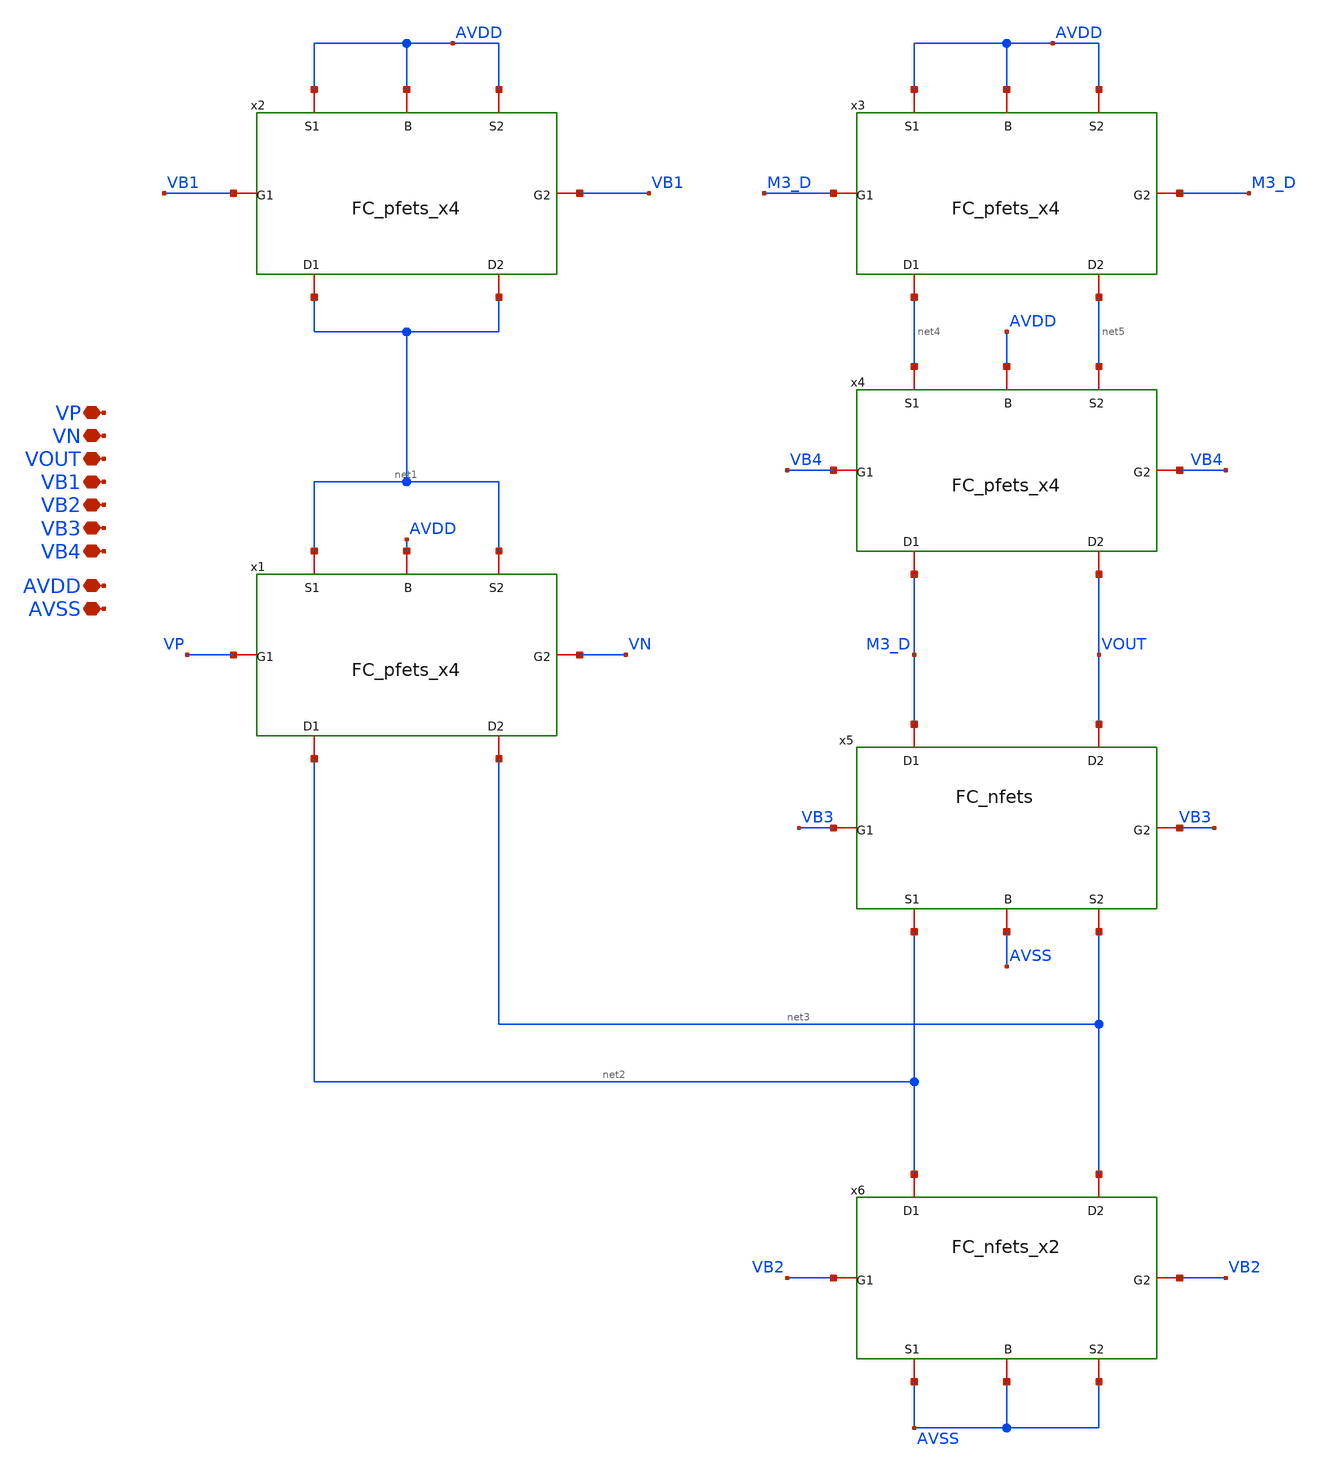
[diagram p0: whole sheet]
** sch_path: TIA_Filter/Folded/FC_net.sch
**.subckt FC_net AVDD AVSS VOUT VP VN VB1 VB2 VB3 VB4
*.iopin AVDD
*.iopin AVSS
*.iopin VOUT
*.iopin VP
*.iopin VN
*.iopin VB1
*.iopin VB2
*.iopin VB3
*.iopin VB4
x1 net1 net1 net2 net3 VP VN AVDD FC_pfets_x4
x2 AVDD AVDD net1 net1 VB1 VB1 AVDD FC_pfets_x4
x3 AVDD AVDD net4 net5 M3_D M3_D AVDD FC_pfets_x4
x4 net4 net5 M3_D VOUT VB4 VB4 AVDD FC_pfets_x4
x5 net2 net3 M3_D VOUT VB3 VB3 AVSS FC_nfets
x6 AVSS AVSS net2 net3 VB2 VB2 AVSS FC_nfets_x2
**.ends

* expanding   symbol:  /home/gmaranhao/Desktop/Bracolin/TIA_Filter/Folded/FC_pfets_x4.sym # of
*+ pins=7
** sym_path: TIA_Filter/Folded/FC_pfets_x4.sym
** sch_path: TIA_Filter/Folded/FC_pfets_x4.sch
.subckt FC_pfets_x4 S1 S2 D1 D2 G1 G2 B
*.iopin S1
*.iopin S2
*.iopin D1
*.iopin D2
*.iopin G1
*.iopin G2
*.iopin B
x1[1] S1 S2 D1 D2 G1 G2 B FC_pfets
x1[2] S1 S2 D1 D2 G1 G2 B FC_pfets
x1[3] S1 S2 D1 D2 G1 G2 B FC_pfets
x1[4] S1 S2 D1 D2 G1 G2 B FC_pfets
.ends


* expanding   symbol:  /home/gmaranhao/Desktop/Bracolin/TIA_Filter/Folded/FC_nfets.sym # of pins=7
** sym_path: TIA_Filter/Folded/FC_nfets.sym
** sch_path: TIA_Filter/Folded/FC_nfets.sch
.subckt FC_nfets S1 S2 D1 D2 G1 G2 B
*.iopin S1
*.iopin S2
*.iopin D1
*.iopin D2
*.iopin G1
*.iopin G2
*.iopin B
XM1[1] D1 G1 S1 B nfet_03v3 L=2u W=2u nf=1 ad='int((nf+1)/2) * W/nf * 0.18u' as='int((nf+2)/2) * W/nf * 0.18u'
+ pd='2*int((nf+1)/2) * (W/nf + 0.18u)' ps='2*int((nf+2)/2) * (W/nf + 0.18u)' nrd='0.18u / W' nrs='0.18u / W'
+ sa=0 sb=0 sd=0 m=1
XM1[2] D1 G1 S1 B nfet_03v3 L=2u W=2u nf=1 ad='int((nf+1)/2) * W/nf * 0.18u' as='int((nf+2)/2) * W/nf * 0.18u'
+ pd='2*int((nf+1)/2) * (W/nf + 0.18u)' ps='2*int((nf+2)/2) * (W/nf + 0.18u)' nrd='0.18u / W' nrs='0.18u / W'
+ sa=0 sb=0 sd=0 m=1
XM1[3] D1 G1 S1 B nfet_03v3 L=2u W=2u nf=1 ad='int((nf+1)/2) * W/nf * 0.18u' as='int((nf+2)/2) * W/nf * 0.18u'
+ pd='2*int((nf+1)/2) * (W/nf + 0.18u)' ps='2*int((nf+2)/2) * (W/nf + 0.18u)' nrd='0.18u / W' nrs='0.18u / W'
+ sa=0 sb=0 sd=0 m=1
XM1[4] D1 G1 S1 B nfet_03v3 L=2u W=2u nf=1 ad='int((nf+1)/2) * W/nf * 0.18u' as='int((nf+2)/2) * W/nf * 0.18u'
+ pd='2*int((nf+1)/2) * (W/nf + 0.18u)' ps='2*int((nf+2)/2) * (W/nf + 0.18u)' nrd='0.18u / W' nrs='0.18u / W'
+ sa=0 sb=0 sd=0 m=1
XM1[5] D1 G1 S1 B nfet_03v3 L=2u W=2u nf=1 ad='int((nf+1)/2) * W/nf * 0.18u' as='int((nf+2)/2) * W/nf * 0.18u'
+ pd='2*int((nf+1)/2) * (W/nf + 0.18u)' ps='2*int((nf+2)/2) * (W/nf + 0.18u)' nrd='0.18u / W' nrs='0.18u / W'
+ sa=0 sb=0 sd=0 m=1
XM1[6] D1 G1 S1 B nfet_03v3 L=2u W=2u nf=1 ad='int((nf+1)/2) * W/nf * 0.18u' as='int((nf+2)/2) * W/nf * 0.18u'
+ pd='2*int((nf+1)/2) * (W/nf + 0.18u)' ps='2*int((nf+2)/2) * (W/nf + 0.18u)' nrd='0.18u / W' nrs='0.18u / W'
+ sa=0 sb=0 sd=0 m=1
XM1[7] D1 G1 S1 B nfet_03v3 L=2u W=2u nf=1 ad='int((nf+1)/2) * W/nf * 0.18u' as='int((nf+2)/2) * W/nf * 0.18u'
+ pd='2*int((nf+1)/2) * (W/nf + 0.18u)' ps='2*int((nf+2)/2) * (W/nf + 0.18u)' nrd='0.18u / W' nrs='0.18u / W'
+ sa=0 sb=0 sd=0 m=1
XM1[8] D1 G1 S1 B nfet_03v3 L=2u W=2u nf=1 ad='int((nf+1)/2) * W/nf * 0.18u' as='int((nf+2)/2) * W/nf * 0.18u'
+ pd='2*int((nf+1)/2) * (W/nf + 0.18u)' ps='2*int((nf+2)/2) * (W/nf + 0.18u)' nrd='0.18u / W' nrs='0.18u / W'
+ sa=0 sb=0 sd=0 m=1
XM1[9] D1 G1 S1 B nfet_03v3 L=2u W=2u nf=1 ad='int((nf+1)/2) * W/nf * 0.18u' as='int((nf+2)/2) * W/nf * 0.18u'
+ pd='2*int((nf+1)/2) * (W/nf + 0.18u)' ps='2*int((nf+2)/2) * (W/nf + 0.18u)' nrd='0.18u / W' nrs='0.18u / W'
+ sa=0 sb=0 sd=0 m=1
XM1[10] D1 G1 S1 B nfet_03v3 L=2u W=2u nf=1 ad='int((nf+1)/2) * W/nf * 0.18u' as='int((nf+2)/2) * W/nf * 0.18u'
+ pd='2*int((nf+1)/2) * (W/nf + 0.18u)' ps='2*int((nf+2)/2) * (W/nf + 0.18u)' nrd='0.18u / W' nrs='0.18u / W'
+ sa=0 sb=0 sd=0 m=1
XM1[11] D1 G1 S1 B nfet_03v3 L=2u W=2u nf=1 ad='int((nf+1)/2) * W/nf * 0.18u' as='int((nf+2)/2) * W/nf * 0.18u'
+ pd='2*int((nf+1)/2) * (W/nf + 0.18u)' ps='2*int((nf+2)/2) * (W/nf + 0.18u)' nrd='0.18u / W' nrs='0.18u / W'
+ sa=0 sb=0 sd=0 m=1
XM1[12] D1 G1 S1 B nfet_03v3 L=2u W=2u nf=1 ad='int((nf+1)/2) * W/nf * 0.18u' as='int((nf+2)/2) * W/nf * 0.18u'
+ pd='2*int((nf+1)/2) * (W/nf + 0.18u)' ps='2*int((nf+2)/2) * (W/nf + 0.18u)' nrd='0.18u / W' nrs='0.18u / W'
+ sa=0 sb=0 sd=0 m=1
XM1[13] D1 G1 S1 B nfet_03v3 L=2u W=2u nf=1 ad='int((nf+1)/2) * W/nf * 0.18u' as='int((nf+2)/2) * W/nf * 0.18u'
+ pd='2*int((nf+1)/2) * (W/nf + 0.18u)' ps='2*int((nf+2)/2) * (W/nf + 0.18u)' nrd='0.18u / W' nrs='0.18u / W'
+ sa=0 sb=0 sd=0 m=1
XM1[14] D1 G1 S1 B nfet_03v3 L=2u W=2u nf=1 ad='int((nf+1)/2) * W/nf * 0.18u' as='int((nf+2)/2) * W/nf * 0.18u'
+ pd='2*int((nf+1)/2) * (W/nf + 0.18u)' ps='2*int((nf+2)/2) * (W/nf + 0.18u)' nrd='0.18u / W' nrs='0.18u / W'
+ sa=0 sb=0 sd=0 m=1
XM1[15] D1 G1 S1 B nfet_03v3 L=2u W=2u nf=1 ad='int((nf+1)/2) * W/nf * 0.18u' as='int((nf+2)/2) * W/nf * 0.18u'
+ pd='2*int((nf+1)/2) * (W/nf + 0.18u)' ps='2*int((nf+2)/2) * (W/nf + 0.18u)' nrd='0.18u / W' nrs='0.18u / W'
+ sa=0 sb=0 sd=0 m=1
XM1[16] D1 G1 S1 B nfet_03v3 L=2u W=2u nf=1 ad='int((nf+1)/2) * W/nf * 0.18u' as='int((nf+2)/2) * W/nf * 0.18u'
+ pd='2*int((nf+1)/2) * (W/nf + 0.18u)' ps='2*int((nf+2)/2) * (W/nf + 0.18u)' nrd='0.18u / W' nrs='0.18u / W'
+ sa=0 sb=0 sd=0 m=1
XM1[17] D1 G1 S1 B nfet_03v3 L=2u W=2u nf=1 ad='int((nf+1)/2) * W/nf * 0.18u' as='int((nf+2)/2) * W/nf * 0.18u'
+ pd='2*int((nf+1)/2) * (W/nf + 0.18u)' ps='2*int((nf+2)/2) * (W/nf + 0.18u)' nrd='0.18u / W' nrs='0.18u / W'
+ sa=0 sb=0 sd=0 m=1
XM1[18] D1 G1 S1 B nfet_03v3 L=2u W=2u nf=1 ad='int((nf+1)/2) * W/nf * 0.18u' as='int((nf+2)/2) * W/nf * 0.18u'
+ pd='2*int((nf+1)/2) * (W/nf + 0.18u)' ps='2*int((nf+2)/2) * (W/nf + 0.18u)' nrd='0.18u / W' nrs='0.18u / W'
+ sa=0 sb=0 sd=0 m=1
XM2[1] D2 G2 S2 B nfet_03v3 L=2u W=2u nf=1 ad='int((nf+1)/2) * W/nf * 0.18u' as='int((nf+2)/2) * W/nf * 0.18u'
+ pd='2*int((nf+1)/2) * (W/nf + 0.18u)' ps='2*int((nf+2)/2) * (W/nf + 0.18u)' nrd='0.18u / W' nrs='0.18u / W'
+ sa=0 sb=0 sd=0 m=1
XM2[2] D2 G2 S2 B nfet_03v3 L=2u W=2u nf=1 ad='int((nf+1)/2) * W/nf * 0.18u' as='int((nf+2)/2) * W/nf * 0.18u'
+ pd='2*int((nf+1)/2) * (W/nf + 0.18u)' ps='2*int((nf+2)/2) * (W/nf + 0.18u)' nrd='0.18u / W' nrs='0.18u / W'
+ sa=0 sb=0 sd=0 m=1
XM2[3] D2 G2 S2 B nfet_03v3 L=2u W=2u nf=1 ad='int((nf+1)/2) * W/nf * 0.18u' as='int((nf+2)/2) * W/nf * 0.18u'
+ pd='2*int((nf+1)/2) * (W/nf + 0.18u)' ps='2*int((nf+2)/2) * (W/nf + 0.18u)' nrd='0.18u / W' nrs='0.18u / W'
+ sa=0 sb=0 sd=0 m=1
XM2[4] D2 G2 S2 B nfet_03v3 L=2u W=2u nf=1 ad='int((nf+1)/2) * W/nf * 0.18u' as='int((nf+2)/2) * W/nf * 0.18u'
+ pd='2*int((nf+1)/2) * (W/nf + 0.18u)' ps='2*int((nf+2)/2) * (W/nf + 0.18u)' nrd='0.18u / W' nrs='0.18u / W'
+ sa=0 sb=0 sd=0 m=1
XM2[5] D2 G2 S2 B nfet_03v3 L=2u W=2u nf=1 ad='int((nf+1)/2) * W/nf * 0.18u' as='int((nf+2)/2) * W/nf * 0.18u'
+ pd='2*int((nf+1)/2) * (W/nf + 0.18u)' ps='2*int((nf+2)/2) * (W/nf + 0.18u)' nrd='0.18u / W' nrs='0.18u / W'
+ sa=0 sb=0 sd=0 m=1
XM2[6] D2 G2 S2 B nfet_03v3 L=2u W=2u nf=1 ad='int((nf+1)/2) * W/nf * 0.18u' as='int((nf+2)/2) * W/nf * 0.18u'
+ pd='2*int((nf+1)/2) * (W/nf + 0.18u)' ps='2*int((nf+2)/2) * (W/nf + 0.18u)' nrd='0.18u / W' nrs='0.18u / W'
+ sa=0 sb=0 sd=0 m=1
XM2[7] D2 G2 S2 B nfet_03v3 L=2u W=2u nf=1 ad='int((nf+1)/2) * W/nf * 0.18u' as='int((nf+2)/2) * W/nf * 0.18u'
+ pd='2*int((nf+1)/2) * (W/nf + 0.18u)' ps='2*int((nf+2)/2) * (W/nf + 0.18u)' nrd='0.18u / W' nrs='0.18u / W'
+ sa=0 sb=0 sd=0 m=1
XM2[8] D2 G2 S2 B nfet_03v3 L=2u W=2u nf=1 ad='int((nf+1)/2) * W/nf * 0.18u' as='int((nf+2)/2) * W/nf * 0.18u'
+ pd='2*int((nf+1)/2) * (W/nf + 0.18u)' ps='2*int((nf+2)/2) * (W/nf + 0.18u)' nrd='0.18u / W' nrs='0.18u / W'
+ sa=0 sb=0 sd=0 m=1
XM2[9] D2 G2 S2 B nfet_03v3 L=2u W=2u nf=1 ad='int((nf+1)/2) * W/nf * 0.18u' as='int((nf+2)/2) * W/nf * 0.18u'
+ pd='2*int((nf+1)/2) * (W/nf + 0.18u)' ps='2*int((nf+2)/2) * (W/nf + 0.18u)' nrd='0.18u / W' nrs='0.18u / W'
+ sa=0 sb=0 sd=0 m=1
XM2[10] D2 G2 S2 B nfet_03v3 L=2u W=2u nf=1 ad='int((nf+1)/2) * W/nf * 0.18u' as='int((nf+2)/2) * W/nf * 0.18u'
+ pd='2*int((nf+1)/2) * (W/nf + 0.18u)' ps='2*int((nf+2)/2) * (W/nf + 0.18u)' nrd='0.18u / W' nrs='0.18u / W'
+ sa=0 sb=0 sd=0 m=1
XM2[11] D2 G2 S2 B nfet_03v3 L=2u W=2u nf=1 ad='int((nf+1)/2) * W/nf * 0.18u' as='int((nf+2)/2) * W/nf * 0.18u'
+ pd='2*int((nf+1)/2) * (W/nf + 0.18u)' ps='2*int((nf+2)/2) * (W/nf + 0.18u)' nrd='0.18u / W' nrs='0.18u / W'
+ sa=0 sb=0 sd=0 m=1
XM2[12] D2 G2 S2 B nfet_03v3 L=2u W=2u nf=1 ad='int((nf+1)/2) * W/nf * 0.18u' as='int((nf+2)/2) * W/nf * 0.18u'
+ pd='2*int((nf+1)/2) * (W/nf + 0.18u)' ps='2*int((nf+2)/2) * (W/nf + 0.18u)' nrd='0.18u / W' nrs='0.18u / W'
+ sa=0 sb=0 sd=0 m=1
XM2[13] D2 G2 S2 B nfet_03v3 L=2u W=2u nf=1 ad='int((nf+1)/2) * W/nf * 0.18u' as='int((nf+2)/2) * W/nf * 0.18u'
+ pd='2*int((nf+1)/2) * (W/nf + 0.18u)' ps='2*int((nf+2)/2) * (W/nf + 0.18u)' nrd='0.18u / W' nrs='0.18u / W'
+ sa=0 sb=0 sd=0 m=1
XM2[14] D2 G2 S2 B nfet_03v3 L=2u W=2u nf=1 ad='int((nf+1)/2) * W/nf * 0.18u' as='int((nf+2)/2) * W/nf * 0.18u'
+ pd='2*int((nf+1)/2) * (W/nf + 0.18u)' ps='2*int((nf+2)/2) * (W/nf + 0.18u)' nrd='0.18u / W' nrs='0.18u / W'
+ sa=0 sb=0 sd=0 m=1
XM2[15] D2 G2 S2 B nfet_03v3 L=2u W=2u nf=1 ad='int((nf+1)/2) * W/nf * 0.18u' as='int((nf+2)/2) * W/nf * 0.18u'
+ pd='2*int((nf+1)/2) * (W/nf + 0.18u)' ps='2*int((nf+2)/2) * (W/nf + 0.18u)' nrd='0.18u / W' nrs='0.18u / W'
+ sa=0 sb=0 sd=0 m=1
XM2[16] D2 G2 S2 B nfet_03v3 L=2u W=2u nf=1 ad='int((nf+1)/2) * W/nf * 0.18u' as='int((nf+2)/2) * W/nf * 0.18u'
+ pd='2*int((nf+1)/2) * (W/nf + 0.18u)' ps='2*int((nf+2)/2) * (W/nf + 0.18u)' nrd='0.18u / W' nrs='0.18u / W'
+ sa=0 sb=0 sd=0 m=1
XM2[17] D2 G2 S2 B nfet_03v3 L=2u W=2u nf=1 ad='int((nf+1)/2) * W/nf * 0.18u' as='int((nf+2)/2) * W/nf * 0.18u'
+ pd='2*int((nf+1)/2) * (W/nf + 0.18u)' ps='2*int((nf+2)/2) * (W/nf + 0.18u)' nrd='0.18u / W' nrs='0.18u / W'
+ sa=0 sb=0 sd=0 m=1
XM2[18] D2 G2 S2 B nfet_03v3 L=2u W=2u nf=1 ad='int((nf+1)/2) * W/nf * 0.18u' as='int((nf+2)/2) * W/nf * 0.18u'
+ pd='2*int((nf+1)/2) * (W/nf + 0.18u)' ps='2*int((nf+2)/2) * (W/nf + 0.18u)' nrd='0.18u / W' nrs='0.18u / W'
+ sa=0 sb=0 sd=0 m=1
.ends


* expanding   symbol:  /home/gmaranhao/Desktop/Bracolin/TIA_Filter/Folded/FC_nfets_x2.sym # of
*+ pins=7
** sym_path: Voltage_Reference/LDO/Folded/FC_nfets_x2.sym
** sch_path: Voltage_Reference/LDO/Folded/FC_nfets_x2.sch
.subckt FC_nfets_x2 S1 S2 D1 D2 G1 G2 B
*.iopin S1
*.iopin S2
*.iopin D1
*.iopin D2
*.iopin G1
*.iopin G2
*.iopin B
x1[1] S1 S2 D1 D2 G1 G2 B FC_nfets
x1[2] S1 S2 D1 D2 G1 G2 B FC_nfets
.ends


* expanding   symbol:  /home/gmaranhao/Desktop/Bracolin/TIA_Filter/Folded/FC_pfets.sym # of pins=7
** sym_path: TIA_Filter/Folded/FC_pfets.sym
** sch_path: TIA_Filter/Folded/FC_pfets.sch
.subckt FC_pfets S1 S2 D1 D2 G1 G2 B
*.iopin S1
*.iopin S2
*.iopin D1
*.iopin D2
*.iopin G1
*.iopin G2
*.iopin B
XM1[1] D1 G1 S1 B pfet_03v3 L=2u W=2u nf=1 ad='int((nf+1)/2) * W/nf * 0.18u' as='int((nf+2)/2) * W/nf * 0.18u'
+ pd='2*int((nf+1)/2) * (W/nf + 0.18u)' ps='2*int((nf+2)/2) * (W/nf + 0.18u)' nrd='0.18u / W' nrs='0.18u / W'
+ sa=0 sb=0 sd=0 m=1
XM1[2] D1 G1 S1 B pfet_03v3 L=2u W=2u nf=1 ad='int((nf+1)/2) * W/nf * 0.18u' as='int((nf+2)/2) * W/nf * 0.18u'
+ pd='2*int((nf+1)/2) * (W/nf + 0.18u)' ps='2*int((nf+2)/2) * (W/nf + 0.18u)' nrd='0.18u / W' nrs='0.18u / W'
+ sa=0 sb=0 sd=0 m=1
XM1[3] D1 G1 S1 B pfet_03v3 L=2u W=2u nf=1 ad='int((nf+1)/2) * W/nf * 0.18u' as='int((nf+2)/2) * W/nf * 0.18u'
+ pd='2*int((nf+1)/2) * (W/nf + 0.18u)' ps='2*int((nf+2)/2) * (W/nf + 0.18u)' nrd='0.18u / W' nrs='0.18u / W'
+ sa=0 sb=0 sd=0 m=1
XM1[4] D1 G1 S1 B pfet_03v3 L=2u W=2u nf=1 ad='int((nf+1)/2) * W/nf * 0.18u' as='int((nf+2)/2) * W/nf * 0.18u'
+ pd='2*int((nf+1)/2) * (W/nf + 0.18u)' ps='2*int((nf+2)/2) * (W/nf + 0.18u)' nrd='0.18u / W' nrs='0.18u / W'
+ sa=0 sb=0 sd=0 m=1
XM1[5] D1 G1 S1 B pfet_03v3 L=2u W=2u nf=1 ad='int((nf+1)/2) * W/nf * 0.18u' as='int((nf+2)/2) * W/nf * 0.18u'
+ pd='2*int((nf+1)/2) * (W/nf + 0.18u)' ps='2*int((nf+2)/2) * (W/nf + 0.18u)' nrd='0.18u / W' nrs='0.18u / W'
+ sa=0 sb=0 sd=0 m=1
XM1[6] D1 G1 S1 B pfet_03v3 L=2u W=2u nf=1 ad='int((nf+1)/2) * W/nf * 0.18u' as='int((nf+2)/2) * W/nf * 0.18u'
+ pd='2*int((nf+1)/2) * (W/nf + 0.18u)' ps='2*int((nf+2)/2) * (W/nf + 0.18u)' nrd='0.18u / W' nrs='0.18u / W'
+ sa=0 sb=0 sd=0 m=1
XM1[7] D1 G1 S1 B pfet_03v3 L=2u W=2u nf=1 ad='int((nf+1)/2) * W/nf * 0.18u' as='int((nf+2)/2) * W/nf * 0.18u'
+ pd='2*int((nf+1)/2) * (W/nf + 0.18u)' ps='2*int((nf+2)/2) * (W/nf + 0.18u)' nrd='0.18u / W' nrs='0.18u / W'
+ sa=0 sb=0 sd=0 m=1
XM1[8] D1 G1 S1 B pfet_03v3 L=2u W=2u nf=1 ad='int((nf+1)/2) * W/nf * 0.18u' as='int((nf+2)/2) * W/nf * 0.18u'
+ pd='2*int((nf+1)/2) * (W/nf + 0.18u)' ps='2*int((nf+2)/2) * (W/nf + 0.18u)' nrd='0.18u / W' nrs='0.18u / W'
+ sa=0 sb=0 sd=0 m=1
XM1[9] D1 G1 S1 B pfet_03v3 L=2u W=2u nf=1 ad='int((nf+1)/2) * W/nf * 0.18u' as='int((nf+2)/2) * W/nf * 0.18u'
+ pd='2*int((nf+1)/2) * (W/nf + 0.18u)' ps='2*int((nf+2)/2) * (W/nf + 0.18u)' nrd='0.18u / W' nrs='0.18u / W'
+ sa=0 sb=0 sd=0 m=1
XM1[10] D1 G1 S1 B pfet_03v3 L=2u W=2u nf=1 ad='int((nf+1)/2) * W/nf * 0.18u' as='int((nf+2)/2) * W/nf * 0.18u'
+ pd='2*int((nf+1)/2) * (W/nf + 0.18u)' ps='2*int((nf+2)/2) * (W/nf + 0.18u)' nrd='0.18u / W' nrs='0.18u / W'
+ sa=0 sb=0 sd=0 m=1
XM1[11] D1 G1 S1 B pfet_03v3 L=2u W=2u nf=1 ad='int((nf+1)/2) * W/nf * 0.18u' as='int((nf+2)/2) * W/nf * 0.18u'
+ pd='2*int((nf+1)/2) * (W/nf + 0.18u)' ps='2*int((nf+2)/2) * (W/nf + 0.18u)' nrd='0.18u / W' nrs='0.18u / W'
+ sa=0 sb=0 sd=0 m=1
XM1[12] D1 G1 S1 B pfet_03v3 L=2u W=2u nf=1 ad='int((nf+1)/2) * W/nf * 0.18u' as='int((nf+2)/2) * W/nf * 0.18u'
+ pd='2*int((nf+1)/2) * (W/nf + 0.18u)' ps='2*int((nf+2)/2) * (W/nf + 0.18u)' nrd='0.18u / W' nrs='0.18u / W'
+ sa=0 sb=0 sd=0 m=1
XM1[13] D1 G1 S1 B pfet_03v3 L=2u W=2u nf=1 ad='int((nf+1)/2) * W/nf * 0.18u' as='int((nf+2)/2) * W/nf * 0.18u'
+ pd='2*int((nf+1)/2) * (W/nf + 0.18u)' ps='2*int((nf+2)/2) * (W/nf + 0.18u)' nrd='0.18u / W' nrs='0.18u / W'
+ sa=0 sb=0 sd=0 m=1
XM1[14] D1 G1 S1 B pfet_03v3 L=2u W=2u nf=1 ad='int((nf+1)/2) * W/nf * 0.18u' as='int((nf+2)/2) * W/nf * 0.18u'
+ pd='2*int((nf+1)/2) * (W/nf + 0.18u)' ps='2*int((nf+2)/2) * (W/nf + 0.18u)' nrd='0.18u / W' nrs='0.18u / W'
+ sa=0 sb=0 sd=0 m=1
XM1[15] D1 G1 S1 B pfet_03v3 L=2u W=2u nf=1 ad='int((nf+1)/2) * W/nf * 0.18u' as='int((nf+2)/2) * W/nf * 0.18u'
+ pd='2*int((nf+1)/2) * (W/nf + 0.18u)' ps='2*int((nf+2)/2) * (W/nf + 0.18u)' nrd='0.18u / W' nrs='0.18u / W'
+ sa=0 sb=0 sd=0 m=1
XM1[16] D1 G1 S1 B pfet_03v3 L=2u W=2u nf=1 ad='int((nf+1)/2) * W/nf * 0.18u' as='int((nf+2)/2) * W/nf * 0.18u'
+ pd='2*int((nf+1)/2) * (W/nf + 0.18u)' ps='2*int((nf+2)/2) * (W/nf + 0.18u)' nrd='0.18u / W' nrs='0.18u / W'
+ sa=0 sb=0 sd=0 m=1
XM1[17] D1 G1 S1 B pfet_03v3 L=2u W=2u nf=1 ad='int((nf+1)/2) * W/nf * 0.18u' as='int((nf+2)/2) * W/nf * 0.18u'
+ pd='2*int((nf+1)/2) * (W/nf + 0.18u)' ps='2*int((nf+2)/2) * (W/nf + 0.18u)' nrd='0.18u / W' nrs='0.18u / W'
+ sa=0 sb=0 sd=0 m=1
XM1[18] D1 G1 S1 B pfet_03v3 L=2u W=2u nf=1 ad='int((nf+1)/2) * W/nf * 0.18u' as='int((nf+2)/2) * W/nf * 0.18u'
+ pd='2*int((nf+1)/2) * (W/nf + 0.18u)' ps='2*int((nf+2)/2) * (W/nf + 0.18u)' nrd='0.18u / W' nrs='0.18u / W'
+ sa=0 sb=0 sd=0 m=1
XM1[19] D1 G1 S1 B pfet_03v3 L=2u W=2u nf=1 ad='int((nf+1)/2) * W/nf * 0.18u' as='int((nf+2)/2) * W/nf * 0.18u'
+ pd='2*int((nf+1)/2) * (W/nf + 0.18u)' ps='2*int((nf+2)/2) * (W/nf + 0.18u)' nrd='0.18u / W' nrs='0.18u / W'
+ sa=0 sb=0 sd=0 m=1
XM1[20] D1 G1 S1 B pfet_03v3 L=2u W=2u nf=1 ad='int((nf+1)/2) * W/nf * 0.18u' as='int((nf+2)/2) * W/nf * 0.18u'
+ pd='2*int((nf+1)/2) * (W/nf + 0.18u)' ps='2*int((nf+2)/2) * (W/nf + 0.18u)' nrd='0.18u / W' nrs='0.18u / W'
+ sa=0 sb=0 sd=0 m=1
XM1[21] D1 G1 S1 B pfet_03v3 L=2u W=2u nf=1 ad='int((nf+1)/2) * W/nf * 0.18u' as='int((nf+2)/2) * W/nf * 0.18u'
+ pd='2*int((nf+1)/2) * (W/nf + 0.18u)' ps='2*int((nf+2)/2) * (W/nf + 0.18u)' nrd='0.18u / W' nrs='0.18u / W'
+ sa=0 sb=0 sd=0 m=1
XM1[22] D1 G1 S1 B pfet_03v3 L=2u W=2u nf=1 ad='int((nf+1)/2) * W/nf * 0.18u' as='int((nf+2)/2) * W/nf * 0.18u'
+ pd='2*int((nf+1)/2) * (W/nf + 0.18u)' ps='2*int((nf+2)/2) * (W/nf + 0.18u)' nrd='0.18u / W' nrs='0.18u / W'
+ sa=0 sb=0 sd=0 m=1
XM2[1] D2 G2 S2 B pfet_03v3 L=2u W=2u nf=1 ad='int((nf+1)/2) * W/nf * 0.18u' as='int((nf+2)/2) * W/nf * 0.18u'
+ pd='2*int((nf+1)/2) * (W/nf + 0.18u)' ps='2*int((nf+2)/2) * (W/nf + 0.18u)' nrd='0.18u / W' nrs='0.18u / W'
+ sa=0 sb=0 sd=0 m=1
XM2[2] D2 G2 S2 B pfet_03v3 L=2u W=2u nf=1 ad='int((nf+1)/2) * W/nf * 0.18u' as='int((nf+2)/2) * W/nf * 0.18u'
+ pd='2*int((nf+1)/2) * (W/nf + 0.18u)' ps='2*int((nf+2)/2) * (W/nf + 0.18u)' nrd='0.18u / W' nrs='0.18u / W'
+ sa=0 sb=0 sd=0 m=1
XM2[3] D2 G2 S2 B pfet_03v3 L=2u W=2u nf=1 ad='int((nf+1)/2) * W/nf * 0.18u' as='int((nf+2)/2) * W/nf * 0.18u'
+ pd='2*int((nf+1)/2) * (W/nf + 0.18u)' ps='2*int((nf+2)/2) * (W/nf + 0.18u)' nrd='0.18u / W' nrs='0.18u / W'
+ sa=0 sb=0 sd=0 m=1
XM2[4] D2 G2 S2 B pfet_03v3 L=2u W=2u nf=1 ad='int((nf+1)/2) * W/nf * 0.18u' as='int((nf+2)/2) * W/nf * 0.18u'
+ pd='2*int((nf+1)/2) * (W/nf + 0.18u)' ps='2*int((nf+2)/2) * (W/nf + 0.18u)' nrd='0.18u / W' nrs='0.18u / W'
+ sa=0 sb=0 sd=0 m=1
XM2[5] D2 G2 S2 B pfet_03v3 L=2u W=2u nf=1 ad='int((nf+1)/2) * W/nf * 0.18u' as='int((nf+2)/2) * W/nf * 0.18u'
+ pd='2*int((nf+1)/2) * (W/nf + 0.18u)' ps='2*int((nf+2)/2) * (W/nf + 0.18u)' nrd='0.18u / W' nrs='0.18u / W'
+ sa=0 sb=0 sd=0 m=1
XM2[6] D2 G2 S2 B pfet_03v3 L=2u W=2u nf=1 ad='int((nf+1)/2) * W/nf * 0.18u' as='int((nf+2)/2) * W/nf * 0.18u'
+ pd='2*int((nf+1)/2) * (W/nf + 0.18u)' ps='2*int((nf+2)/2) * (W/nf + 0.18u)' nrd='0.18u / W' nrs='0.18u / W'
+ sa=0 sb=0 sd=0 m=1
XM2[7] D2 G2 S2 B pfet_03v3 L=2u W=2u nf=1 ad='int((nf+1)/2) * W/nf * 0.18u' as='int((nf+2)/2) * W/nf * 0.18u'
+ pd='2*int((nf+1)/2) * (W/nf + 0.18u)' ps='2*int((nf+2)/2) * (W/nf + 0.18u)' nrd='0.18u / W' nrs='0.18u / W'
+ sa=0 sb=0 sd=0 m=1
XM2[8] D2 G2 S2 B pfet_03v3 L=2u W=2u nf=1 ad='int((nf+1)/2) * W/nf * 0.18u' as='int((nf+2)/2) * W/nf * 0.18u'
+ pd='2*int((nf+1)/2) * (W/nf + 0.18u)' ps='2*int((nf+2)/2) * (W/nf + 0.18u)' nrd='0.18u / W' nrs='0.18u / W'
+ sa=0 sb=0 sd=0 m=1
XM2[9] D2 G2 S2 B pfet_03v3 L=2u W=2u nf=1 ad='int((nf+1)/2) * W/nf * 0.18u' as='int((nf+2)/2) * W/nf * 0.18u'
+ pd='2*int((nf+1)/2) * (W/nf + 0.18u)' ps='2*int((nf+2)/2) * (W/nf + 0.18u)' nrd='0.18u / W' nrs='0.18u / W'
+ sa=0 sb=0 sd=0 m=1
XM2[10] D2 G2 S2 B pfet_03v3 L=2u W=2u nf=1 ad='int((nf+1)/2) * W/nf * 0.18u' as='int((nf+2)/2) * W/nf * 0.18u'
+ pd='2*int((nf+1)/2) * (W/nf + 0.18u)' ps='2*int((nf+2)/2) * (W/nf + 0.18u)' nrd='0.18u / W' nrs='0.18u / W'
+ sa=0 sb=0 sd=0 m=1
XM2[11] D2 G2 S2 B pfet_03v3 L=2u W=2u nf=1 ad='int((nf+1)/2) * W/nf * 0.18u' as='int((nf+2)/2) * W/nf * 0.18u'
+ pd='2*int((nf+1)/2) * (W/nf + 0.18u)' ps='2*int((nf+2)/2) * (W/nf + 0.18u)' nrd='0.18u / W' nrs='0.18u / W'
+ sa=0 sb=0 sd=0 m=1
XM2[12] D2 G2 S2 B pfet_03v3 L=2u W=2u nf=1 ad='int((nf+1)/2) * W/nf * 0.18u' as='int((nf+2)/2) * W/nf * 0.18u'
+ pd='2*int((nf+1)/2) * (W/nf + 0.18u)' ps='2*int((nf+2)/2) * (W/nf + 0.18u)' nrd='0.18u / W' nrs='0.18u / W'
+ sa=0 sb=0 sd=0 m=1
XM2[13] D2 G2 S2 B pfet_03v3 L=2u W=2u nf=1 ad='int((nf+1)/2) * W/nf * 0.18u' as='int((nf+2)/2) * W/nf * 0.18u'
+ pd='2*int((nf+1)/2) * (W/nf + 0.18u)' ps='2*int((nf+2)/2) * (W/nf + 0.18u)' nrd='0.18u / W' nrs='0.18u / W'
+ sa=0 sb=0 sd=0 m=1
XM2[14] D2 G2 S2 B pfet_03v3 L=2u W=2u nf=1 ad='int((nf+1)/2) * W/nf * 0.18u' as='int((nf+2)/2) * W/nf * 0.18u'
+ pd='2*int((nf+1)/2) * (W/nf + 0.18u)' ps='2*int((nf+2)/2) * (W/nf + 0.18u)' nrd='0.18u / W' nrs='0.18u / W'
+ sa=0 sb=0 sd=0 m=1
XM2[15] D2 G2 S2 B pfet_03v3 L=2u W=2u nf=1 ad='int((nf+1)/2) * W/nf * 0.18u' as='int((nf+2)/2) * W/nf * 0.18u'
+ pd='2*int((nf+1)/2) * (W/nf + 0.18u)' ps='2*int((nf+2)/2) * (W/nf + 0.18u)' nrd='0.18u / W' nrs='0.18u / W'
+ sa=0 sb=0 sd=0 m=1
XM2[16] D2 G2 S2 B pfet_03v3 L=2u W=2u nf=1 ad='int((nf+1)/2) * W/nf * 0.18u' as='int((nf+2)/2) * W/nf * 0.18u'
+ pd='2*int((nf+1)/2) * (W/nf + 0.18u)' ps='2*int((nf+2)/2) * (W/nf + 0.18u)' nrd='0.18u / W' nrs='0.18u / W'
+ sa=0 sb=0 sd=0 m=1
XM2[17] D2 G2 S2 B pfet_03v3 L=2u W=2u nf=1 ad='int((nf+1)/2) * W/nf * 0.18u' as='int((nf+2)/2) * W/nf * 0.18u'
+ pd='2*int((nf+1)/2) * (W/nf + 0.18u)' ps='2*int((nf+2)/2) * (W/nf + 0.18u)' nrd='0.18u / W' nrs='0.18u / W'
+ sa=0 sb=0 sd=0 m=1
XM2[18] D2 G2 S2 B pfet_03v3 L=2u W=2u nf=1 ad='int((nf+1)/2) * W/nf * 0.18u' as='int((nf+2)/2) * W/nf * 0.18u'
+ pd='2*int((nf+1)/2) * (W/nf + 0.18u)' ps='2*int((nf+2)/2) * (W/nf + 0.18u)' nrd='0.18u / W' nrs='0.18u / W'
+ sa=0 sb=0 sd=0 m=1
XM2[19] D2 G2 S2 B pfet_03v3 L=2u W=2u nf=1 ad='int((nf+1)/2) * W/nf * 0.18u' as='int((nf+2)/2) * W/nf * 0.18u'
+ pd='2*int((nf+1)/2) * (W/nf + 0.18u)' ps='2*int((nf+2)/2) * (W/nf + 0.18u)' nrd='0.18u / W' nrs='0.18u / W'
+ sa=0 sb=0 sd=0 m=1
XM2[20] D2 G2 S2 B pfet_03v3 L=2u W=2u nf=1 ad='int((nf+1)/2) * W/nf * 0.18u' as='int((nf+2)/2) * W/nf * 0.18u'
+ pd='2*int((nf+1)/2) * (W/nf + 0.18u)' ps='2*int((nf+2)/2) * (W/nf + 0.18u)' nrd='0.18u / W' nrs='0.18u / W'
+ sa=0 sb=0 sd=0 m=1
XM2[21] D2 G2 S2 B pfet_03v3 L=2u W=2u nf=1 ad='int((nf+1)/2) * W/nf * 0.18u' as='int((nf+2)/2) * W/nf * 0.18u'
+ pd='2*int((nf+1)/2) * (W/nf + 0.18u)' ps='2*int((nf+2)/2) * (W/nf + 0.18u)' nrd='0.18u / W' nrs='0.18u / W'
+ sa=0 sb=0 sd=0 m=1
XM2[22] D2 G2 S2 B pfet_03v3 L=2u W=2u nf=1 ad='int((nf+1)/2) * W/nf * 0.18u' as='int((nf+2)/2) * W/nf * 0.18u'
+ pd='2*int((nf+1)/2) * (W/nf + 0.18u)' ps='2*int((nf+2)/2) * (W/nf + 0.18u)' nrd='0.18u / W' nrs='0.18u / W'
+ sa=0 sb=0 sd=0 m=1
.ends

.end
